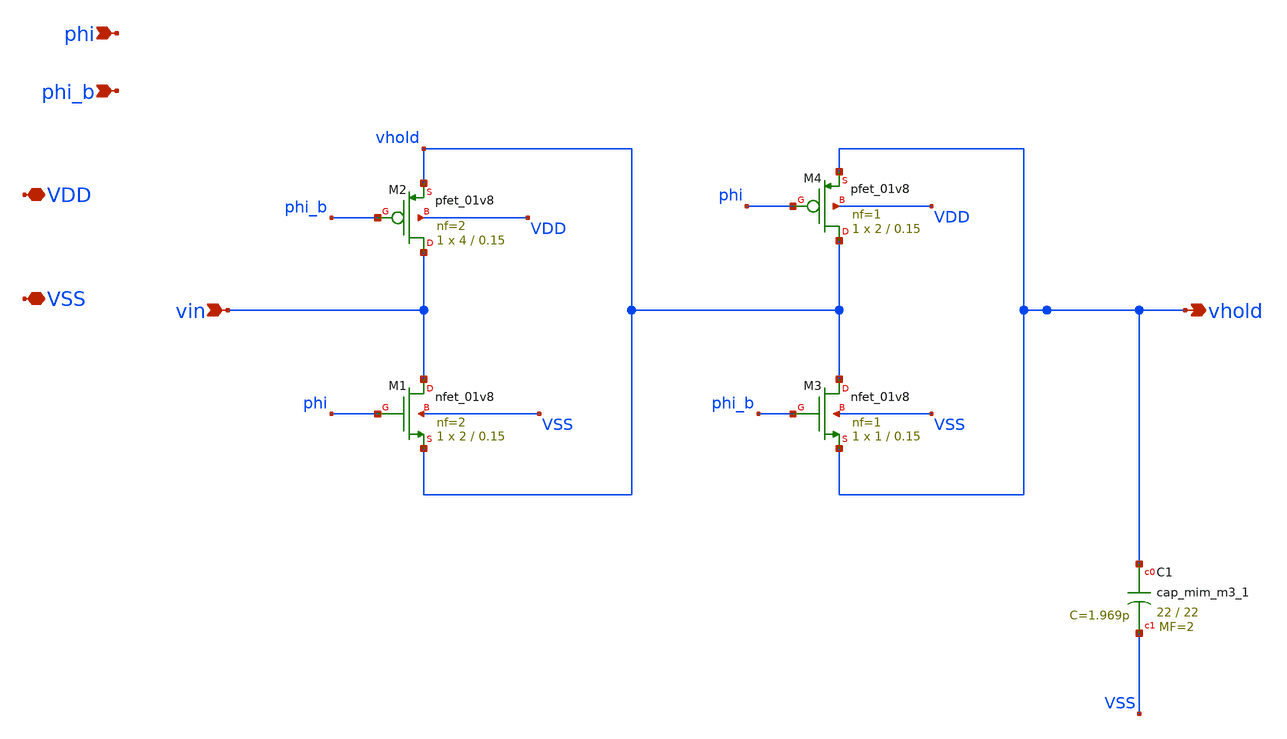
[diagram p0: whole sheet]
** sch_path: xschem/sample_hold.sch
**.subckt sample_hold VDD VSS vhold phi_b phi vin
*.iopin VDD
*.iopin VSS
*.opin vhold
*.ipin phi_b
*.ipin phi
*.ipin vin
XM2 vin phi_b vhold VDD sky130_fd_pr__pfet_01v8 L=0.15 W=4 nf=2 ad='int((2 + 1)/2) * 4 / 2 * 0.29' as='int((2 + 2)/2) * 4 / 2 * 0.29'
+ pd='2*int((2 + 1)/2) * (4 / 2 + 0.29)' ps='2*int((2 + 2)/2) * (4 / 2 + 0.29)' nrd='0.29 / 4 ' nrs='0.29 / 4 '
+ sa=0 sb=0 sd=0 mult=1 m=1
XM4 vhold phi vhold VDD sky130_fd_pr__pfet_01v8 L=0.15 W=2 nf=1 ad='int((1 + 1)/2) * 2 / 1 * 0.29' as='int((1 + 2)/2) * 2 / 1 * 0.29'
+ pd='2*int((1 + 1)/2) * (2 / 1 + 0.29)' ps='2*int((1 + 2)/2) * (2 / 1 + 0.29)' nrd='0.29 / 2 ' nrs='0.29 / 2 '
+ sa=0 sb=0 sd=0 mult=1 m=1
XM1 vin phi vhold VSS sky130_fd_pr__nfet_01v8 L=0.15 W=2 nf=2 ad='int((2 + 1)/2) * 2 / 2 * 0.29' as='int((2 + 2)/2) * 2 / 2 * 0.29'
+ pd='2*int((2 + 1)/2) * (2 / 2 + 0.29)' ps='2*int((2 + 2)/2) * (2 / 2 + 0.29)' nrd='0.29 / 2 ' nrs='0.29 / 2 '
+ sa=0 sb=0 sd=0 mult=1 m=1
XM3 vhold phi_b vhold VSS sky130_fd_pr__nfet_01v8 L=0.15 W=1 nf=1 ad='int((1 + 1)/2) * 1 / 1 * 0.29'
+ as='int((1 + 2)/2) * 1 / 1 * 0.29' pd='2*int((1 + 1)/2) * (1 / 1 + 0.29)' ps='2*int((1 + 2)/2) * (1 / 1 + 0.29)'
+ nrd='0.29 / 1 ' nrs='0.29 / 1 ' sa=0 sb=0 sd=0 mult=1 m=1
XC1 vhold VSS sky130_fd_pr__cap_mim_m3_1 W=22 L=22 MF=2 m=2
**.ends
.end
